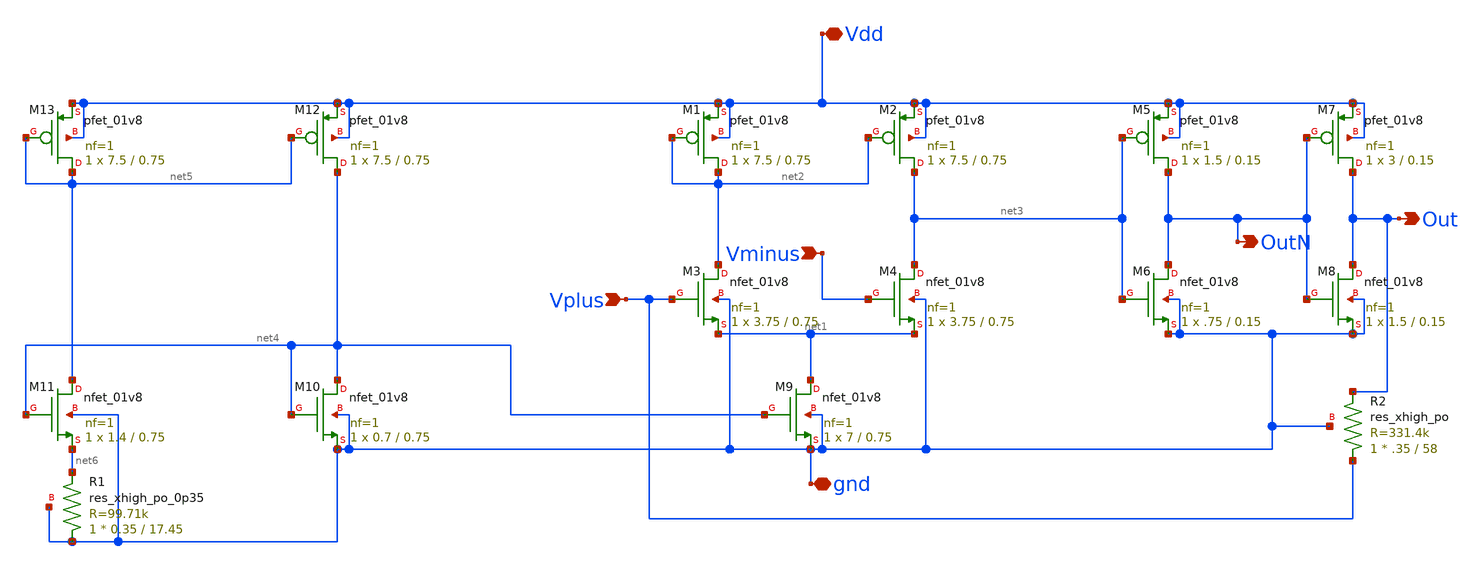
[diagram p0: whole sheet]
** sch_path: xschem/comparator.sch
**.subckt comparator Vminus Vplus Vdd gnd OutN Out
*.ipin Vminus
*.ipin Vplus
*.iopin Vdd
*.iopin gnd
*.opin OutN
*.opin Out
XM1 net2 net2 Vdd Vdd sky130_fd_pr__pfet_01v8 L=0.75 W=7.5 nf=1 ad='int((nf+1)/2) * W/nf * 0.29' as='int((nf+2)/2) * W/nf * 0.29'
+ pd='2*int((nf+1)/2) * (W/nf + 0.29)' ps='2*int((nf+2)/2) * (W/nf + 0.29)' nrd='0.29 / W' nrs='0.29 / W'
+ sa=0 sb=0 sd=0 mult=1 m=1
XM2 net3 net2 Vdd Vdd sky130_fd_pr__pfet_01v8 L=0.75 W=7.5 nf=1 ad='int((nf+1)/2) * W/nf * 0.29' as='int((nf+2)/2) * W/nf * 0.29'
+ pd='2*int((nf+1)/2) * (W/nf + 0.29)' ps='2*int((nf+2)/2) * (W/nf + 0.29)' nrd='0.29 / W' nrs='0.29 / W'
+ sa=0 sb=0 sd=0 mult=1 m=1
XM5 OutN net3 Vdd Vdd sky130_fd_pr__pfet_01v8 L=0.15 W=1.5 nf=1 ad='int((nf+1)/2) * W/nf * 0.29' as='int((nf+2)/2) * W/nf * 0.29'
+ pd='2*int((nf+1)/2) * (W/nf + 0.29)' ps='2*int((nf+2)/2) * (W/nf + 0.29)' nrd='0.29 / W' nrs='0.29 / W'
+ sa=0 sb=0 sd=0 mult=1 m=1
XM6 OutN net3 gnd gnd sky130_fd_pr__nfet_01v8 L=0.15 W=.75 nf=1 ad='int((nf+1)/2) * W/nf * 0.29' as='int((nf+2)/2) * W/nf * 0.29'
+ pd='2*int((nf+1)/2) * (W/nf + 0.29)' ps='2*int((nf+2)/2) * (W/nf + 0.29)' nrd='0.29 / W' nrs='0.29 / W'
+ sa=0 sb=0 sd=0 mult=1 m=1
XM7 Out OutN Vdd Vdd sky130_fd_pr__pfet_01v8 L=0.15 W=3 nf=1 ad='int((nf+1)/2) * W/nf * 0.29' as='int((nf+2)/2) * W/nf * 0.29'
+ pd='2*int((nf+1)/2) * (W/nf + 0.29)' ps='2*int((nf+2)/2) * (W/nf + 0.29)' nrd='0.29 / W' nrs='0.29 / W'
+ sa=0 sb=0 sd=0 mult=1 m=1
XM8 Out OutN gnd gnd sky130_fd_pr__nfet_01v8 L=0.15 W=1.5 nf=1 ad='int((nf+1)/2) * W/nf * 0.29' as='int((nf+2)/2) * W/nf * 0.29'
+ pd='2*int((nf+1)/2) * (W/nf + 0.29)' ps='2*int((nf+2)/2) * (W/nf + 0.29)' nrd='0.29 / W' nrs='0.29 / W'
+ sa=0 sb=0 sd=0 mult=1 m=1
XM3 net2 Vplus net1 gnd sky130_fd_pr__nfet_01v8 L=0.75 W=3.75 nf=1 ad='int((nf+1)/2) * W/nf * 0.29' as='int((nf+2)/2) * W/nf * 0.29'
+ pd='2*int((nf+1)/2) * (W/nf + 0.29)' ps='2*int((nf+2)/2) * (W/nf + 0.29)' nrd='0.29 / W' nrs='0.29 / W'
+ sa=0 sb=0 sd=0 mult=1 m=1
XM4 net3 Vminus net1 gnd sky130_fd_pr__nfet_01v8 L=0.75 W=3.75 nf=1 ad='int((nf+1)/2) * W/nf * 0.29'
+ as='int((nf+2)/2) * W/nf * 0.29' pd='2*int((nf+1)/2) * (W/nf + 0.29)' ps='2*int((nf+2)/2) * (W/nf + 0.29)'
+ nrd='0.29 / W' nrs='0.29 / W' sa=0 sb=0 sd=0 mult=1 m=1
XM9 net1 net4 gnd gnd sky130_fd_pr__nfet_01v8 L=0.75 W=7 nf=1 ad='int((nf+1)/2) * W/nf * 0.29' as='int((nf+2)/2) * W/nf * 0.29'
+ pd='2*int((nf+1)/2) * (W/nf + 0.29)' ps='2*int((nf+2)/2) * (W/nf + 0.29)' nrd='0.29 / W' nrs='0.29 / W'
+ sa=0 sb=0 sd=0 mult=1 m=1
XM10 net4 net4 gnd gnd sky130_fd_pr__nfet_01v8 L=0.75 W=0.7 nf=1 ad='int((nf+1)/2) * W/nf * 0.29' as='int((nf+2)/2) * W/nf * 0.29'
+ pd='2*int((nf+1)/2) * (W/nf + 0.29)' ps='2*int((nf+2)/2) * (W/nf + 0.29)' nrd='0.29 / W' nrs='0.29 / W'
+ sa=0 sb=0 sd=0 mult=1 m=1
XM11 net5 net4 net6 gnd sky130_fd_pr__nfet_01v8 L=0.75 W=1.4 nf=1 ad='int((nf+1)/2) * W/nf * 0.29' as='int((nf+2)/2) * W/nf * 0.29'
+ pd='2*int((nf+1)/2) * (W/nf + 0.29)' ps='2*int((nf+2)/2) * (W/nf + 0.29)' nrd='0.29 / W' nrs='0.29 / W'
+ sa=0 sb=0 sd=0 mult=1 m=1
XM12 net4 net5 Vdd Vdd sky130_fd_pr__pfet_01v8 L=0.75 W=7.5 nf=1 ad='int((nf+1)/2) * W/nf * 0.29' as='int((nf+2)/2) * W/nf * 0.29'
+ pd='2*int((nf+1)/2) * (W/nf + 0.29)' ps='2*int((nf+2)/2) * (W/nf + 0.29)' nrd='0.29 / W' nrs='0.29 / W'
+ sa=0 sb=0 sd=0 mult=1 m=1
XM13 net5 net5 Vdd Vdd sky130_fd_pr__pfet_01v8 L=0.75 W=7.5 nf=1 ad='int((nf+1)/2) * W/nf * 0.29' as='int((nf+2)/2) * W/nf * 0.29'
+ pd='2*int((nf+1)/2) * (W/nf + 0.29)' ps='2*int((nf+2)/2) * (W/nf + 0.29)' nrd='0.29 / W' nrs='0.29 / W'
+ sa=0 sb=0 sd=0 mult=1 m=1
XR1 gnd net6 gnd sky130_fd_pr__res_xhigh_po_0p35 L=17.45 mult=1 m=1
XR2 Vplus Out gnd sky130_fd_pr__res_xhigh_po W=.35 L=58 mult=1 m=1
**.ends
.end
